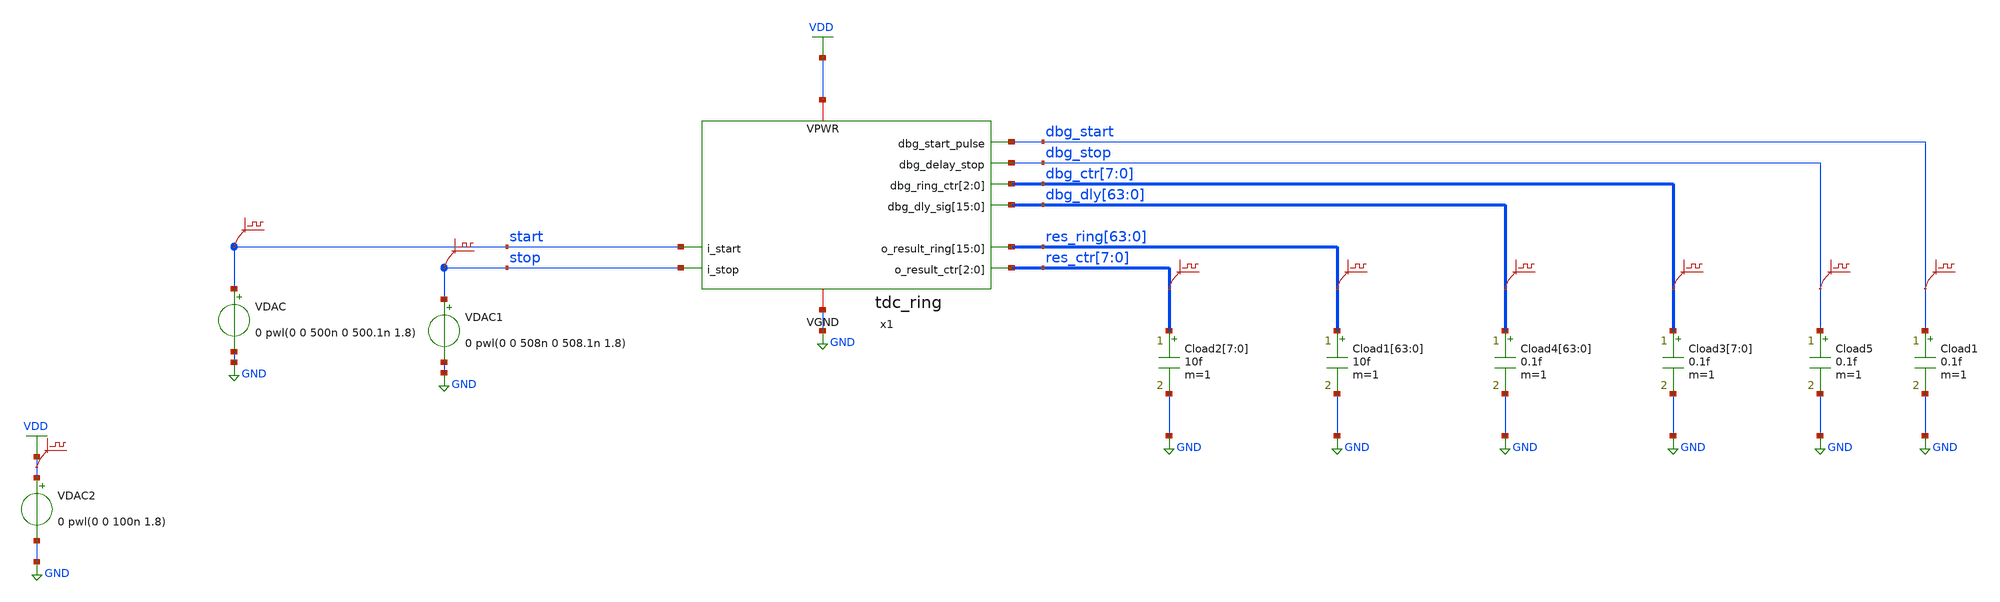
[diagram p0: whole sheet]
** sch_path: sim/tb_tt06_tdc.sch
**.subckt tb_tt06_tdc
VDAC start GND 0 pwl(0 0 500n 0 500.1n 1.8)
.save v(start)
VDAC1 stop GND 0 pwl(0 0 508n 0 508.1n 1.8)
.save v(stop)
Cload1[63] res_ring[63] GND 10f m=1
Cload1[62] res_ring[62] GND 10f m=1
Cload1[61] res_ring[61] GND 10f m=1
Cload1[60] res_ring[60] GND 10f m=1
Cload1[59] res_ring[59] GND 10f m=1
Cload1[58] res_ring[58] GND 10f m=1
Cload1[57] res_ring[57] GND 10f m=1
Cload1[56] res_ring[56] GND 10f m=1
Cload1[55] res_ring[55] GND 10f m=1
Cload1[54] res_ring[54] GND 10f m=1
Cload1[53] res_ring[53] GND 10f m=1
Cload1[52] res_ring[52] GND 10f m=1
Cload1[51] res_ring[51] GND 10f m=1
Cload1[50] res_ring[50] GND 10f m=1
Cload1[49] res_ring[49] GND 10f m=1
Cload1[48] res_ring[48] GND 10f m=1
Cload1[47] res_ring[47] GND 10f m=1
Cload1[46] res_ring[46] GND 10f m=1
Cload1[45] res_ring[45] GND 10f m=1
Cload1[44] res_ring[44] GND 10f m=1
Cload1[43] res_ring[43] GND 10f m=1
Cload1[42] res_ring[42] GND 10f m=1
Cload1[41] res_ring[41] GND 10f m=1
Cload1[40] res_ring[40] GND 10f m=1
Cload1[39] res_ring[39] GND 10f m=1
Cload1[38] res_ring[38] GND 10f m=1
Cload1[37] res_ring[37] GND 10f m=1
Cload1[36] res_ring[36] GND 10f m=1
Cload1[35] res_ring[35] GND 10f m=1
Cload1[34] res_ring[34] GND 10f m=1
Cload1[33] res_ring[33] GND 10f m=1
Cload1[32] res_ring[32] GND 10f m=1
Cload1[31] res_ring[31] GND 10f m=1
Cload1[30] res_ring[30] GND 10f m=1
Cload1[29] res_ring[29] GND 10f m=1
Cload1[28] res_ring[28] GND 10f m=1
Cload1[27] res_ring[27] GND 10f m=1
Cload1[26] res_ring[26] GND 10f m=1
Cload1[25] res_ring[25] GND 10f m=1
Cload1[24] res_ring[24] GND 10f m=1
Cload1[23] res_ring[23] GND 10f m=1
Cload1[22] res_ring[22] GND 10f m=1
Cload1[21] res_ring[21] GND 10f m=1
Cload1[20] res_ring[20] GND 10f m=1
Cload1[19] res_ring[19] GND 10f m=1
Cload1[18] res_ring[18] GND 10f m=1
Cload1[17] res_ring[17] GND 10f m=1
Cload1[16] res_ring[16] GND 10f m=1
Cload1[15] res_ring[15] GND 10f m=1
Cload1[14] res_ring[14] GND 10f m=1
Cload1[13] res_ring[13] GND 10f m=1
Cload1[12] res_ring[12] GND 10f m=1
Cload1[11] res_ring[11] GND 10f m=1
Cload1[10] res_ring[10] GND 10f m=1
Cload1[9] res_ring[9] GND 10f m=1
Cload1[8] res_ring[8] GND 10f m=1
Cload1[7] res_ring[7] GND 10f m=1
Cload1[6] res_ring[6] GND 10f m=1
Cload1[5] res_ring[5] GND 10f m=1
Cload1[4] res_ring[4] GND 10f m=1
Cload1[3] res_ring[3] GND 10f m=1
Cload1[2] res_ring[2] GND 10f m=1
Cload1[1] res_ring[1] GND 10f m=1
Cload1[0] res_ring[0] GND 10f m=1
.save v(res_ring[63])
.save v(res_ring[62])
.save v(res_ring[61])
.save v(res_ring[60])
.save v(res_ring[59])
.save v(res_ring[58])
.save v(res_ring[57])
.save v(res_ring[56])
.save v(res_ring[55])
.save v(res_ring[54])
.save v(res_ring[53])
.save v(res_ring[52])
.save v(res_ring[51])
.save v(res_ring[50])
.save v(res_ring[49])
.save v(res_ring[48])
.save v(res_ring[47])
.save v(res_ring[46])
.save v(res_ring[45])
.save v(res_ring[44])
.save v(res_ring[43])
.save v(res_ring[42])
.save v(res_ring[41])
.save v(res_ring[40])
.save v(res_ring[39])
.save v(res_ring[38])
.save v(res_ring[37])
.save v(res_ring[36])
.save v(res_ring[35])
.save v(res_ring[34])
.save v(res_ring[33])
.save v(res_ring[32])
.save v(res_ring[31])
.save v(res_ring[30])
.save v(res_ring[29])
.save v(res_ring[28])
.save v(res_ring[27])
.save v(res_ring[26])
.save v(res_ring[25])
.save v(res_ring[24])
.save v(res_ring[23])
.save v(res_ring[22])
.save v(res_ring[21])
.save v(res_ring[20])
.save v(res_ring[19])
.save v(res_ring[18])
.save v(res_ring[17])
.save v(res_ring[16])
.save v(res_ring[15])
.save v(res_ring[14])
.save v(res_ring[13])
.save v(res_ring[12])
.save v(res_ring[11])
.save v(res_ring[10])
.save v(res_ring[9])
.save v(res_ring[8])
.save v(res_ring[7])
.save v(res_ring[6])
.save v(res_ring[5])
.save v(res_ring[4])
.save v(res_ring[3])
.save v(res_ring[2])
.save v(res_ring[1])
.save v(res_ring[0])
.save v(vdd)
VDAC2 VDD GND 0 pwl(0 0 100n 1.8)
Cload2[7] res_ctr[7] GND 10f m=1
Cload2[6] res_ctr[6] GND 10f m=1
Cload2[5] res_ctr[5] GND 10f m=1
Cload2[4] res_ctr[4] GND 10f m=1
Cload2[3] res_ctr[3] GND 10f m=1
Cload2[2] res_ctr[2] GND 10f m=1
Cload2[1] res_ctr[1] GND 10f m=1
Cload2[0] res_ctr[0] GND 10f m=1
.save v(res_ctr[7])
.save v(res_ctr[6])
.save v(res_ctr[5])
.save v(res_ctr[4])
.save v(res_ctr[3])
.save v(res_ctr[2])
.save v(res_ctr[1])
.save v(res_ctr[0])
x1 start stop res_ring[63] res_ring[62] res_ring[61] res_ring[60] res_ring[59] res_ring[58]
+ res_ring[57] res_ring[56] res_ring[55] res_ring[54] res_ring[53] res_ring[52] res_ring[51] res_ring[50]
+ res_ring[49] res_ring[48] res_ctr[7] res_ctr[6] res_ctr[5] dbg_start dbg_stop dbg_ctr[7] dbg_ctr[6] dbg_ctr[5]
+ dbg_dly[63] dbg_dly[62] dbg_dly[61] dbg_dly[60] dbg_dly[59] dbg_dly[58] dbg_dly[57] dbg_dly[56] dbg_dly[55]
+ dbg_dly[54] dbg_dly[53] dbg_dly[52] dbg_dly[51] dbg_dly[50] dbg_dly[49] dbg_dly[48] VDD GND tdc_ring
Cload3[7] dbg_ctr[7] GND 0.1f m=1
Cload3[6] dbg_ctr[6] GND 0.1f m=1
Cload3[5] dbg_ctr[5] GND 0.1f m=1
Cload3[4] dbg_ctr[4] GND 0.1f m=1
Cload3[3] dbg_ctr[3] GND 0.1f m=1
Cload3[2] dbg_ctr[2] GND 0.1f m=1
Cload3[1] dbg_ctr[1] GND 0.1f m=1
Cload3[0] dbg_ctr[0] GND 0.1f m=1
Cload4[63] dbg_dly[63] GND 0.1f m=1
Cload4[62] dbg_dly[62] GND 0.1f m=1
Cload4[61] dbg_dly[61] GND 0.1f m=1
Cload4[60] dbg_dly[60] GND 0.1f m=1
Cload4[59] dbg_dly[59] GND 0.1f m=1
Cload4[58] dbg_dly[58] GND 0.1f m=1
Cload4[57] dbg_dly[57] GND 0.1f m=1
Cload4[56] dbg_dly[56] GND 0.1f m=1
Cload4[55] dbg_dly[55] GND 0.1f m=1
Cload4[54] dbg_dly[54] GND 0.1f m=1
Cload4[53] dbg_dly[53] GND 0.1f m=1
Cload4[52] dbg_dly[52] GND 0.1f m=1
Cload4[51] dbg_dly[51] GND 0.1f m=1
Cload4[50] dbg_dly[50] GND 0.1f m=1
Cload4[49] dbg_dly[49] GND 0.1f m=1
Cload4[48] dbg_dly[48] GND 0.1f m=1
Cload4[47] dbg_dly[47] GND 0.1f m=1
Cload4[46] dbg_dly[46] GND 0.1f m=1
Cload4[45] dbg_dly[45] GND 0.1f m=1
Cload4[44] dbg_dly[44] GND 0.1f m=1
Cload4[43] dbg_dly[43] GND 0.1f m=1
Cload4[42] dbg_dly[42] GND 0.1f m=1
Cload4[41] dbg_dly[41] GND 0.1f m=1
Cload4[40] dbg_dly[40] GND 0.1f m=1
Cload4[39] dbg_dly[39] GND 0.1f m=1
Cload4[38] dbg_dly[38] GND 0.1f m=1
Cload4[37] dbg_dly[37] GND 0.1f m=1
Cload4[36] dbg_dly[36] GND 0.1f m=1
Cload4[35] dbg_dly[35] GND 0.1f m=1
Cload4[34] dbg_dly[34] GND 0.1f m=1
Cload4[33] dbg_dly[33] GND 0.1f m=1
Cload4[32] dbg_dly[32] GND 0.1f m=1
Cload4[31] dbg_dly[31] GND 0.1f m=1
Cload4[30] dbg_dly[30] GND 0.1f m=1
Cload4[29] dbg_dly[29] GND 0.1f m=1
Cload4[28] dbg_dly[28] GND 0.1f m=1
Cload4[27] dbg_dly[27] GND 0.1f m=1
Cload4[26] dbg_dly[26] GND 0.1f m=1
Cload4[25] dbg_dly[25] GND 0.1f m=1
Cload4[24] dbg_dly[24] GND 0.1f m=1
Cload4[23] dbg_dly[23] GND 0.1f m=1
Cload4[22] dbg_dly[22] GND 0.1f m=1
Cload4[21] dbg_dly[21] GND 0.1f m=1
Cload4[20] dbg_dly[20] GND 0.1f m=1
Cload4[19] dbg_dly[19] GND 0.1f m=1
Cload4[18] dbg_dly[18] GND 0.1f m=1
Cload4[17] dbg_dly[17] GND 0.1f m=1
Cload4[16] dbg_dly[16] GND 0.1f m=1
Cload4[15] dbg_dly[15] GND 0.1f m=1
Cload4[14] dbg_dly[14] GND 0.1f m=1
Cload4[13] dbg_dly[13] GND 0.1f m=1
Cload4[12] dbg_dly[12] GND 0.1f m=1
Cload4[11] dbg_dly[11] GND 0.1f m=1
Cload4[10] dbg_dly[10] GND 0.1f m=1
Cload4[9] dbg_dly[9] GND 0.1f m=1
Cload4[8] dbg_dly[8] GND 0.1f m=1
Cload4[7] dbg_dly[7] GND 0.1f m=1
Cload4[6] dbg_dly[6] GND 0.1f m=1
Cload4[5] dbg_dly[5] GND 0.1f m=1
Cload4[4] dbg_dly[4] GND 0.1f m=1
Cload4[3] dbg_dly[3] GND 0.1f m=1
Cload4[2] dbg_dly[2] GND 0.1f m=1
Cload4[1] dbg_dly[1] GND 0.1f m=1
Cload4[0] dbg_dly[0] GND 0.1f m=1
.save v(dbg_dly[63])
.save v(dbg_dly[62])
.save v(dbg_dly[61])
.save v(dbg_dly[60])
.save v(dbg_dly[59])
.save v(dbg_dly[58])
.save v(dbg_dly[57])
.save v(dbg_dly[56])
.save v(dbg_dly[55])
.save v(dbg_dly[54])
.save v(dbg_dly[53])
.save v(dbg_dly[52])
.save v(dbg_dly[51])
.save v(dbg_dly[50])
.save v(dbg_dly[49])
.save v(dbg_dly[48])
.save v(dbg_dly[47])
.save v(dbg_dly[46])
.save v(dbg_dly[45])
.save v(dbg_dly[44])
.save v(dbg_dly[43])
.save v(dbg_dly[42])
.save v(dbg_dly[41])
.save v(dbg_dly[40])
.save v(dbg_dly[39])
.save v(dbg_dly[38])
.save v(dbg_dly[37])
.save v(dbg_dly[36])
.save v(dbg_dly[35])
.save v(dbg_dly[34])
.save v(dbg_dly[33])
.save v(dbg_dly[32])
.save v(dbg_dly[31])
.save v(dbg_dly[30])
.save v(dbg_dly[29])
.save v(dbg_dly[28])
.save v(dbg_dly[27])
.save v(dbg_dly[26])
.save v(dbg_dly[25])
.save v(dbg_dly[24])
.save v(dbg_dly[23])
.save v(dbg_dly[22])
.save v(dbg_dly[21])
.save v(dbg_dly[20])
.save v(dbg_dly[19])
.save v(dbg_dly[18])
.save v(dbg_dly[17])
.save v(dbg_dly[16])
.save v(dbg_dly[15])
.save v(dbg_dly[14])
.save v(dbg_dly[13])
.save v(dbg_dly[12])
.save v(dbg_dly[11])
.save v(dbg_dly[10])
.save v(dbg_dly[9])
.save v(dbg_dly[8])
.save v(dbg_dly[7])
.save v(dbg_dly[6])
.save v(dbg_dly[5])
.save v(dbg_dly[4])
.save v(dbg_dly[3])
.save v(dbg_dly[2])
.save v(dbg_dly[1])
.save v(dbg_dly[0])
.save v(dbg_ctr[7])
.save v(dbg_ctr[6])
.save v(dbg_ctr[5])
.save v(dbg_ctr[4])
.save v(dbg_ctr[3])
.save v(dbg_ctr[2])
.save v(dbg_ctr[1])
.save v(dbg_ctr[0])
Cload5 dbg_stop GND 0.1f m=1
Cload1 dbg_start GND 0.1f m=1
.save v(dbg_stop)
.save v(dbg_start)
**** begin user architecture code



* ngspice commands
****************

****************
* Misc
****************
.param fclk=10MEG
.options method=gear maxord=2
.temp 30

.control
set num_threads=6
tran 0.01n 600n

write tb_tt06_tdc.raw

*exit
.endc




** opencircuitdesign pdks install
.lib $::SKYWATER_MODELS/sky130.lib.spice tt


**** end user architecture code
**.ends

* expanding   symbol:  /foss/designs/sim/tdc_ring.sym # of pins=10
** sym_path: sim/tdc_ring.sym
.include tdc_ring.pex.spice
.GLOBAL VDD
.GLOBAL GND
.end
